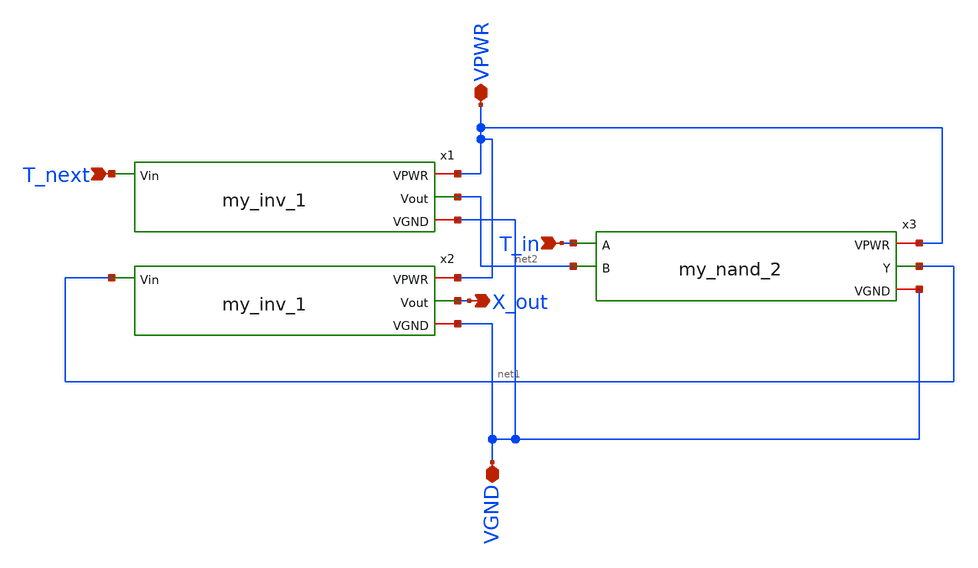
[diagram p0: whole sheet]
** sch_path: edge_cell.sch
**.subckt edge_cell T_next T_in X_out VPWR VGND
*.ipin T_next
*.ipin T_in
*.opin X_out
*.iopin VPWR
*.iopin VGND
x1 VPWR T_next net2 VGND my_inv_1
x2 VPWR net1 X_out VGND my_inv_1
x3 VPWR net1 T_in net2 VGND my_nand_2
**.ends

* expanding   symbol:  /home/huydq/my_inv_1.sym # of pins=4
** sym_path: my_inv_1.sym
** sch_path: my_inv_1.sch
.subckt my_inv_1 VPWR Vin Vout VGND
*.iopin VGND
*.iopin VPWR
*.ipin Vin
*.opin Vout
XM1 Vout Vin VGND VGND sky130_fd_pr__nfet_g5v0d10v5 L=0.5 W=1 nf=1 ad='int((nf+1)/2) * W/nf * 0.29' as='int((nf+2)/2) * W/nf * 0.29'
+ pd='2*int((nf+1)/2) * (W/nf + 0.29)' ps='2*int((nf+2)/2) * (W/nf + 0.29)' nrd='0.29 / W' nrs='0.29 / W'
+ sa=0 sb=0 sd=0 mult=1 m=1
XM2 Vout Vin VPWR VPWR sky130_fd_pr__pfet_g5v0d10v5 L=0.5 W=1 nf=1 ad='int((nf+1)/2) * W/nf * 0.29' as='int((nf+2)/2) * W/nf * 0.29'
+ pd='2*int((nf+1)/2) * (W/nf + 0.29)' ps='2*int((nf+2)/2) * (W/nf + 0.29)' nrd='0.29 / W' nrs='0.29 / W'
+ sa=0 sb=0 sd=0 mult=1 m=1
.ends


* expanding   symbol:  /home/huydq/my_nand_2.sym # of pins=5
** sym_path: my_nand_2.sym
** sch_path: my_nand_2.sch
.subckt my_nand_2 VPWR Y A B VGND
*.iopin VPWR
*.iopin VGND
*.ipin A
*.ipin B
*.opin Y
XM5 Y B net1 VGND sky130_fd_pr__nfet_g5v0d10v5 L=0.5 W=1 nf=1 ad='int((nf+1)/2) * W/nf * 0.29' as='int((nf+2)/2) * W/nf * 0.29'
+ pd='2*int((nf+1)/2) * (W/nf + 0.29)' ps='2*int((nf+2)/2) * (W/nf + 0.29)' nrd='0.29 / W' nrs='0.29 / W'
+ sa=0 sb=0 sd=0 mult=1 m=1
XM6 Y B VPWR VPWR sky130_fd_pr__pfet_g5v0d10v5 L=0.5 W=1 nf=1 ad='int((nf+1)/2) * W/nf * 0.29' as='int((nf+2)/2) * W/nf * 0.29'
+ pd='2*int((nf+1)/2) * (W/nf + 0.29)' ps='2*int((nf+2)/2) * (W/nf + 0.29)' nrd='0.29 / W' nrs='0.29 / W'
+ sa=0 sb=0 sd=0 mult=1 m=1
XM2 Y A VPWR VPWR sky130_fd_pr__pfet_g5v0d10v5 L=0.5 W=1 nf=1 ad='int((nf+1)/2) * W/nf * 0.29' as='int((nf+2)/2) * W/nf * 0.29'
+ pd='2*int((nf+1)/2) * (W/nf + 0.29)' ps='2*int((nf+2)/2) * (W/nf + 0.29)' nrd='0.29 / W' nrs='0.29 / W'
+ sa=0 sb=0 sd=0 mult=1 m=1
XM1 net1 A VGND VGND sky130_fd_pr__nfet_g5v0d10v5 L=0.5 W=1 nf=1 ad='int((nf+1)/2) * W/nf * 0.29' as='int((nf+2)/2) * W/nf * 0.29'
+ pd='2*int((nf+1)/2) * (W/nf + 0.29)' ps='2*int((nf+2)/2) * (W/nf + 0.29)' nrd='0.29 / W' nrs='0.29 / W'
+ sa=0 sb=0 sd=0 mult=1 m=1
.ends

.end
